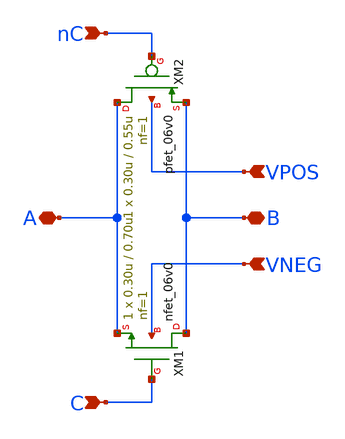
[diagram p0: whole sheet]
** sch_path: xschem/blocks/transmission_gate/transmission_gate.sch
**.subckt transmission_gate A B C nC VPOS VNEG
*.iopin A
*.iopin B
*.ipin C
*.ipin nC
*.ipin VPOS
*.ipin VNEG
XM1 B C A VNEG nfet_06v0 L=0.70u W=0.30u nf=1 ad='int((nf+1)/2) * W/nf * 0.18u' as='int((nf+2)/2) * W/nf * 0.18u'
+ pd='2*int((nf+1)/2) * (W/nf + 0.18u)' ps='2*int((nf+2)/2) * (W/nf + 0.18u)' nrd='0.18u / W' nrs='0.18u / W'
+ sa=0 sb=0 sd=0 m=1
XM2 A nC B VPOS pfet_06v0 L=0.55u W=0.30u nf=1 ad='int((nf+1)/2) * W/nf * 0.18u' as='int((nf+2)/2) * W/nf * 0.18u'
+ pd='2*int((nf+1)/2) * (W/nf + 0.18u)' ps='2*int((nf+2)/2) * (W/nf + 0.18u)' nrd='0.18u / W' nrs='0.18u / W'
+ sa=0 sb=0 sd=0 m=1
**.ends
.end
